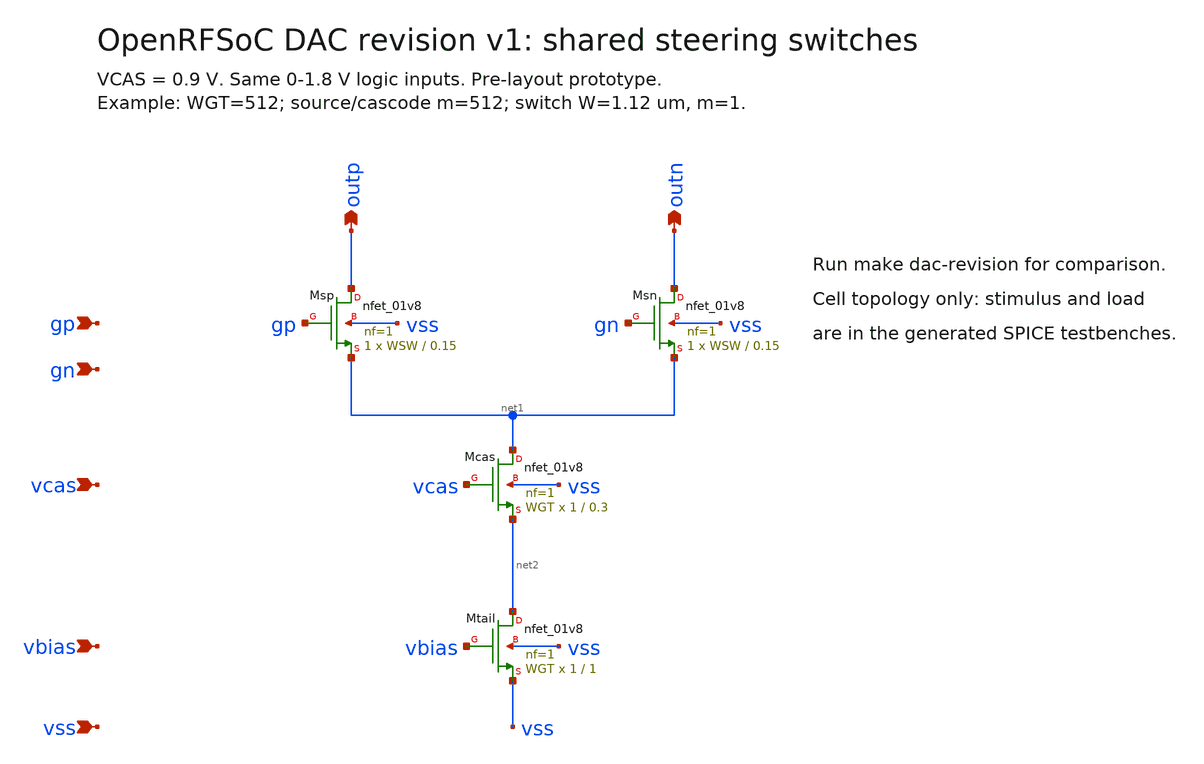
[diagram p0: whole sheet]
** sch_path: analog/dac14_2g/current_cell_shared.sch
**.subckt current_cell_shared outp outn gp gn vcas vbias vss
*.opin outp
*.opin outn
*.ipin gp
*.ipin gn
*.ipin vcas
*.ipin vbias
*.ipin vss
XMsp outp gp net1 vss sky130_fd_pr__nfet_01v8 L=0.15 W=WSW nf=1 ad='int((1 + 1)/2) * WSW / 1 * 0.29'
+ as='int((1 + 2)/2) * WSW / 1 * 0.29' pd='2*int((1 + 1)/2) * (WSW / 1 + 0.29)' ps='2*int((1 + 2)/2) * (WSW / 1 + 0.29)'
+ nrd='0.14/WSW' nrs='0.14/WSW' sa=0 sb=0 sd=0 mult=1 m=1
XMsn outn gn net1 vss sky130_fd_pr__nfet_01v8 L=0.15 W=WSW nf=1 ad='int((1 + 1)/2) * WSW / 1 * 0.29'
+ as='int((1 + 2)/2) * WSW / 1 * 0.29' pd='2*int((1 + 1)/2) * (WSW / 1 + 0.29)' ps='2*int((1 + 2)/2) * (WSW / 1 + 0.29)'
+ nrd='0.14/WSW' nrs='0.14/WSW' sa=0 sb=0 sd=0 mult=1 m=1
XMcas net1 vcas net2 vss sky130_fd_pr__nfet_01v8 L=0.3 W=1 nf=1 ad='int((1 + 1)/2) * 1 / 1 * 0.29' as='int((1 + 2)/2) * 1 / 1 * 0.29'
+ pd='2*int((1 + 1)/2) * (1 / 1 + 0.29)' ps='2*int((1 + 2)/2) * (1 / 1 + 0.29)' nrd=0.14 nrs=0.14 sa=0
+ sb=0 sd=0 mult=WGT m=WGT
XMtail net2 vbias vss vss sky130_fd_pr__nfet_01v8 L=1 W=1 nf=1 ad='int((1 + 1)/2) * 1 / 1 * 0.29' as='int((1 + 2)/2) * 1 / 1 * 0.29'
+ pd='2*int((1 + 1)/2) * (1 / 1 + 0.29)' ps='2*int((1 + 2)/2) * (1 / 1 + 0.29)' nrd=0.14 nrs=0.14 sa=0
+ sb=0 sd=0 mult=WGT m=WGT
**** begin user architecture code

.param WGT=512 SWDIV=192 WSW='max(0.42,0.42*WGT/SWDIV)'

**** end user architecture code
**.ends
.end
